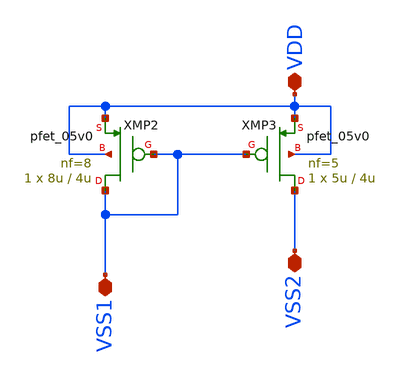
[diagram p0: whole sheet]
** sch_path: xschem/vco/vco_pmosmirr_forlvs.sch
**.subckt vco_pmosmirr_forlvs VDD VSS1 VSS2
*.iopin VDD
*.iopin VSS1
*.iopin VSS2
XMP2 VSS1 VSS1 VDD VDD pfet_05v0 L=4u W=8u nf=8 ad='int((nf+1)/2) * W/nf * 0.18u' as='int((nf+2)/2) * W/nf * 0.18u'
+ pd='2*int((nf+1)/2) * (W/nf + 0.18u)' ps='2*int((nf+2)/2) * (W/nf + 0.18u)' nrd='0.18u / W' nrs='0.18u / W'
+ sa=0 sb=0 sd=0 m=1
XMP3 VSS2 VSS1 VDD VDD pfet_05v0 L=4u W=5u nf=5 ad='int((nf+1)/2) * W/nf * 0.18u' as='int((nf+2)/2) * W/nf * 0.18u'
+ pd='2*int((nf+1)/2) * (W/nf + 0.18u)' ps='2*int((nf+2)/2) * (W/nf + 0.18u)' nrd='0.18u / W' nrs='0.18u / W'
+ sa=0 sb=0 sd=0 m=1
**.ends
.end
